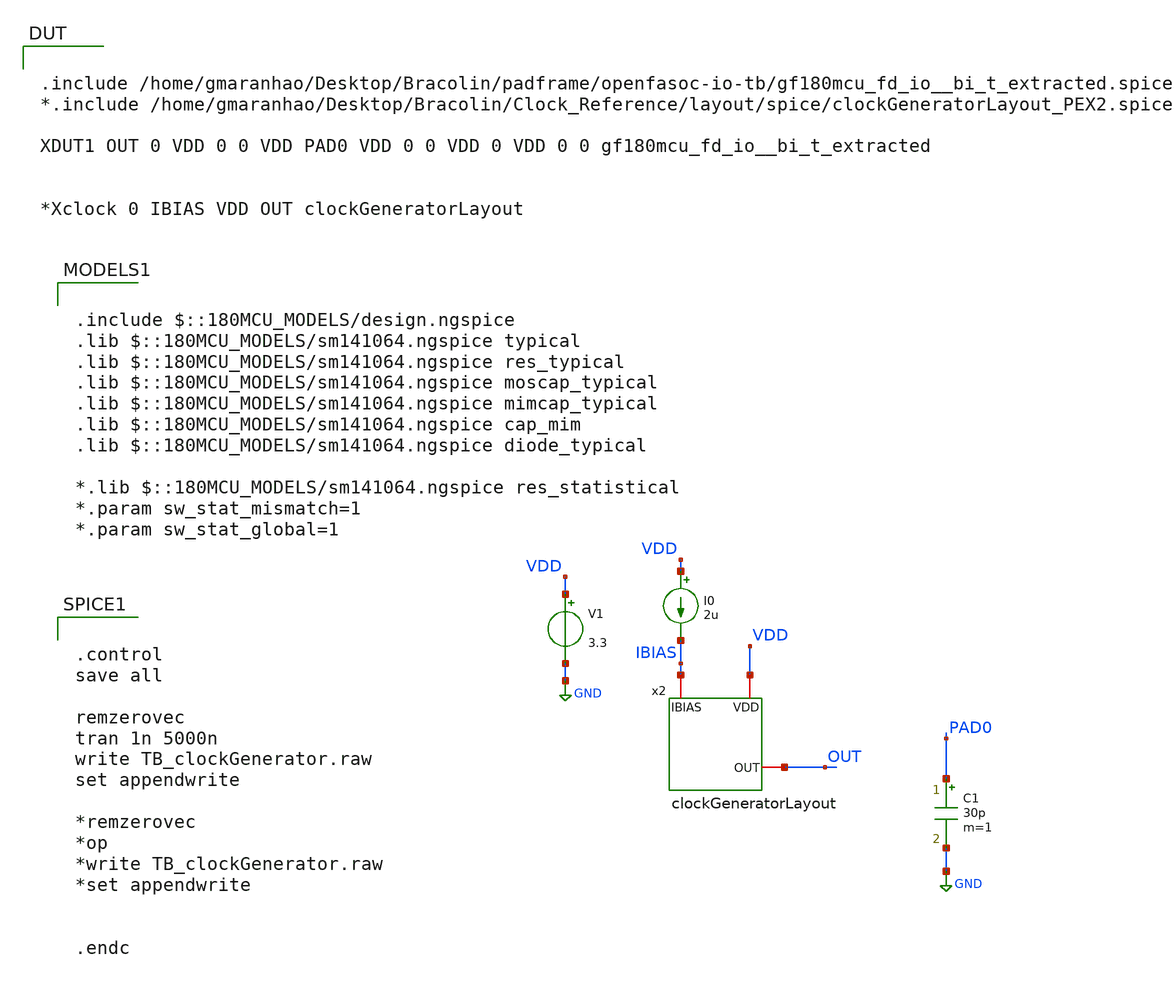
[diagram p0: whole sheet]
** sch_path: Clock_Reference/TB_clockGenerator.sch
**.subckt TB_clockGenerator
I0 VDD IBIAS 2u
V1 VDD GND 3.3
x2 VDD OUT IBIAS clockGeneratorLayout
C1 PAD0 GND 30p m=1
**** begin user architecture code


.control
save all

remzerovec
tran 1n 5000n
write TB_clockGenerator.raw
set appendwrite

*remzerovec
*op
*write TB_clockGenerator.raw
*set appendwrite


.endc




.include $::180MCU_MODELS/design.ngspice
.lib $::180MCU_MODELS/sm141064.ngspice typical
.lib $::180MCU_MODELS/sm141064.ngspice res_typical
.lib $::180MCU_MODELS/sm141064.ngspice moscap_typical
.lib $::180MCU_MODELS/sm141064.ngspice mimcap_typical
.lib $::180MCU_MODELS/sm141064.ngspice cap_mim
.lib $::180MCU_MODELS/sm141064.ngspice diode_typical

*.lib $::180MCU_MODELS/sm141064.ngspice res_statistical
*.param sw_stat_mismatch=1
*.param sw_stat_global=1



.include /home/gmaranhao/Desktop/Bracolin/padframe/openfasoc-io-tb/gf180mcu_fd_io__bi_t_extracted.spice
*.include /home/gmaranhao/Desktop/Bracolin/Clock_Reference/layout/spice/clockGeneratorLayout_PEX2.spice

XDUT1 OUT 0 VDD 0 0 VDD PAD0 VDD 0 0 VDD 0 VDD 0 0 gf180mcu_fd_io__bi_t_extracted


*Xclock 0 IBIAS VDD OUT clockGeneratorLayout

**** end user architecture code
**.ends
.GLOBAL GND
.end
